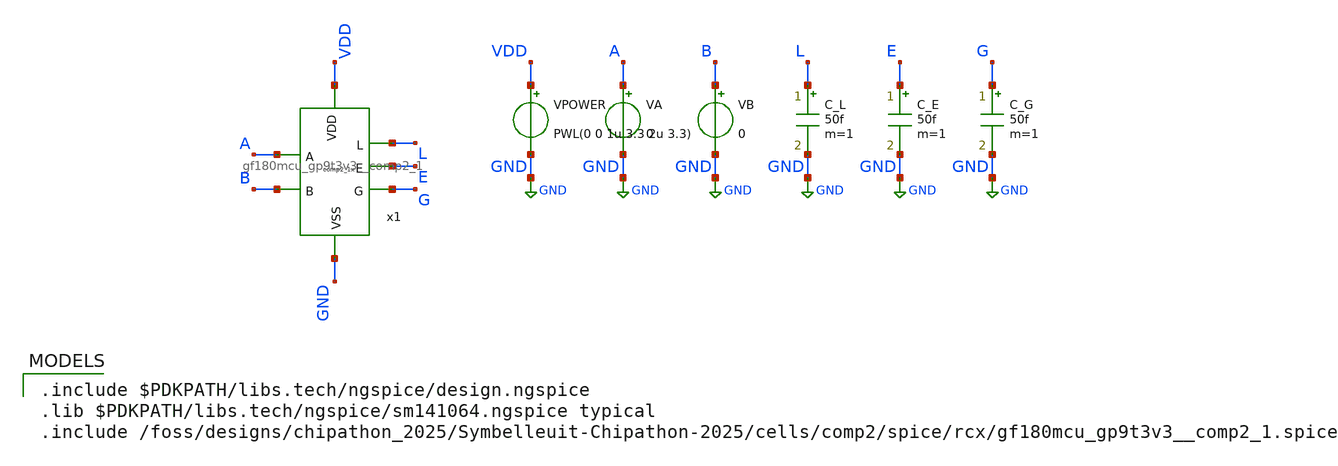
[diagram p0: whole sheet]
** sch_path: cells/comp2/cace/templates/comp2_tb_powerup.sch
**.subckt comp2_tb_powerup
x1 VDD L A E G B GND gf180mcu_gp9t3v3__comp2_1
VPOWER VDD GND PWL(0 0 1u 3.3 2u 3.3)
.save i(vpower)
VA A GND 0
VB B GND 0
C_L L GND 50f m=1
C_E E GND 50f m=1
C_G G GND 50f m=1
**** begin user architecture code

.include $PDKPATH/libs.tech/ngspice/design.ngspice
.lib $PDKPATH/libs.tech/ngspice/sm141064.ngspice typical
.include /foss/designs/chipathon_2025/Symbelleuit-Chipathon-2025/cells/comp2/spice/rcx/gf180mcu_gp9t3v3__comp2_1.spice


* CACE Power-Up Inrush Current Simulation
.tran 20n 2u
.control
  run
  let idd = -i(VPOWER)
  meas tran i_inrush MAX idd from=0 to=2u
  print i_inrush
  echo $&i_inrush > comp2_tb_powerup_0.data
.endc
.GLOBAL GND


**** end user architecture code
**.ends
.GLOBAL GND
.end
